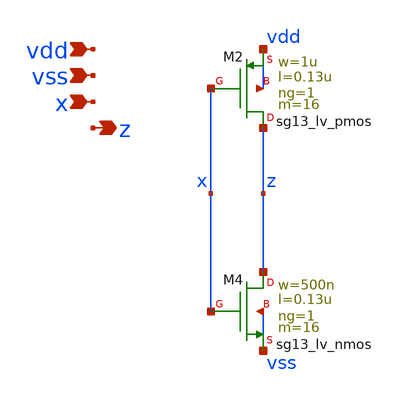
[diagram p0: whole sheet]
** sch_path: MSPHY9932-main/sch/buf_16.sch
**.subckt buf_16 vdd vss x z
*.ipin vdd
*.ipin vss
*.ipin x
*.opin z
XM2 z x vdd vdd sg13_lv_pmos w=1u l=0.13u ng=1 m=16 mm_ok=1
XM4 z x vss vss sg13_lv_nmos w=500n l=0.13u ng=1 m=16 mm_ok=1
**.ends
.end
